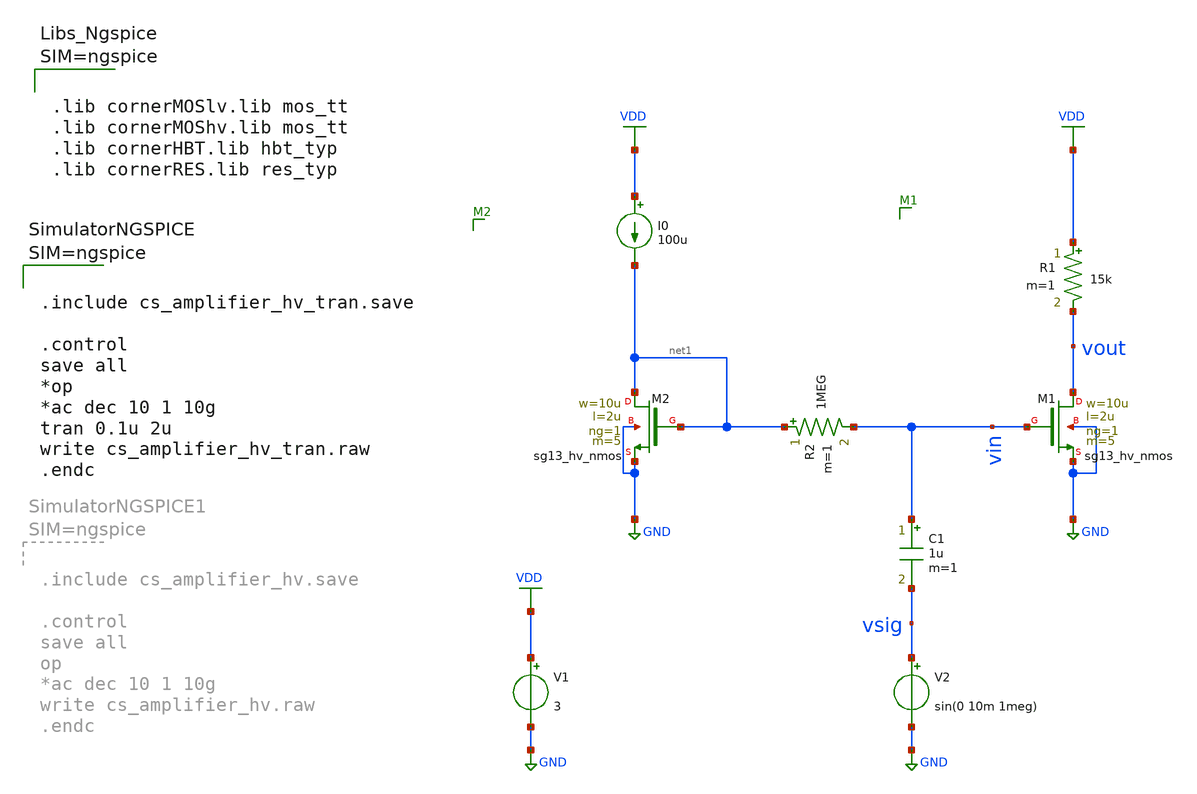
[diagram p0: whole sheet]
** sch_path: Schematics/lab_1/cs_amplifier_hv_tran.sch
**.subckt cs_amplifier_hv_tran
R1 VDD vout 15k m=1
I0 VDD net1 100u
V1 VDD GND 3
V2 vsig GND sin(0 10m 1meg)
XM1 vout vin GND GND sg13_hv_nmos w=10u l=2u ng=1 m=5 mm_ok=1
XM2 net1 net1 GND GND sg13_hv_nmos w=10u l=2u ng=1 m=5 mm_ok=1
R2 net1 vin 1MEG m=1
C1 vin vsig 1u m=1
**** begin user architecture code



.lib cornerMOSlv.lib mos_tt
.lib cornerMOShv.lib mos_tt
.lib cornerHBT.lib hbt_typ
.lib cornerRES.lib res_typ






.include cs_amplifier_hv_tran.save

.control
save all
*op
*ac dec 10 1 10g
tran 0.1u 2u
write cs_amplifier_hv_tran.raw
.endc



**** end user architecture code
**.ends
.GLOBAL GND
.GLOBAL VDD
.end
